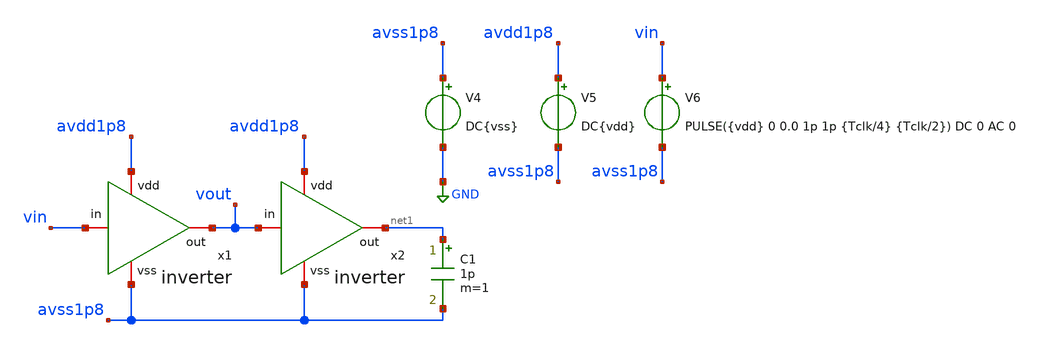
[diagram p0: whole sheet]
** sch_path: verification/testbenches/inverter/tb_inverter.sch
**.subckt tb_inverter
x1 avdd1p8 vout vin avss1p8 inverter
x2 avdd1p8 net1 vout avss1p8 inverter
C1 net1 avss1p8 1p m=1
V4 avss1p8 GND DC{vss}
V5 avdd1p8 avss1p8 DC{vdd}
V6 vin avss1p8 PULSE({vdd} 0 0.0 1p 1p {Tclk/4} {Tclk/2}) DC 0 AC 0
**** begin user architecture code


* Circuit Parameters
.param vdd = 1.8
.param vss = 0.0
.param Tclk = 10n
.options TEMP = 65.0
* Include Models
.lib /foss/pdks/sky130A/libs.tech/ngspice/sky130.lib.spice TT
* OP Parameters & Singals to save
.save all
*Simulations
.control
tran 0.01u 100n
setplot tran1
plot v(vin) v(vout)+2
reset
dc V6 0 1.8 0.01
setplot dc
plot vin vout ylabel vout xlabel vin
set filetype = ascii
write dcsweep.raw
.endc
.end


**** end user architecture code
**.ends

* expanding   symbol:  blocks/inverter/schematic/inverter.sym # of pins=4
** sym_path: design/blocks/inverter/schematic/inverter.sym
** sch_path: design/blocks/inverter/schematic/inverter.sch
.subckt inverter vdd out in vss
*.iopin vdd
*.iopin out
*.iopin vss
*.iopin in
XM1 out in vss vss sky130_fd_pr__nfet_01v8 L=0.15 W=0.75 nf=1 ad='int((nf+1)/2) * W/nf * 0.29' as='int((nf+2)/2) * W/nf * 0.29'
+ pd='2*int((nf+1)/2) * (W/nf + 0.29)' ps='2*int((nf+2)/2) * (W/nf + 0.29)' nrd='0.29 / W' nrs='0.29 / W'
+ sa=0 sb=0 sd=0 mult=1 m=1
XM2 out in vdd vdd sky130_fd_pr__pfet_01v8 L=0.15 W=1.5 nf=1 ad='int((nf+1)/2) * W/nf * 0.29' as='int((nf+2)/2) * W/nf * 0.29'
+ pd='2*int((nf+1)/2) * (W/nf + 0.29)' ps='2*int((nf+2)/2) * (W/nf + 0.29)' nrd='0.29 / W' nrs='0.29 / W'
+ sa=0 sb=0 sd=0 mult=1 m=1
.ends

.GLOBAL GND
.end
